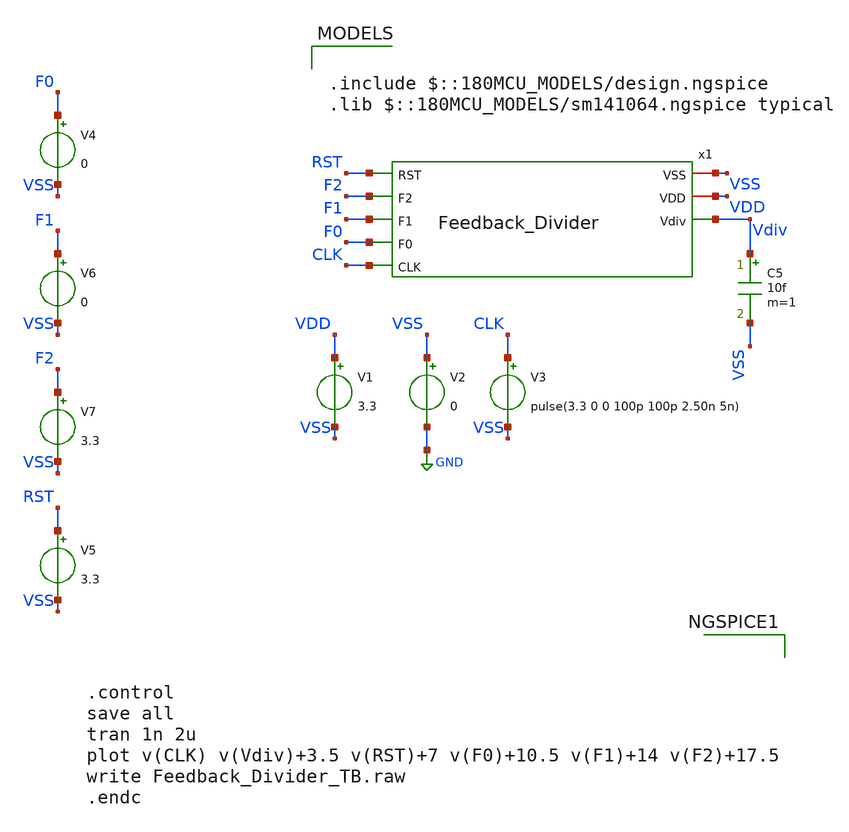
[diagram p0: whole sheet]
** sch_path: Clock_Generator_PAKISTAN_02/Schematics/delete.sch
**.subckt delete
V1 VDD VSS 3.3
V2 VSS GND 0
V3 CLK VSS pulse(3.3 0 0 100p 100p 2.50n 5n)
C5 Vdiv VSS 10f m=1
V5 RST VSS 3.3
x1 VSS VDD RST Vdiv F2 F1 F0 CLK Feedback_Divider
V4 F0 VSS 0
V6 F1 VSS 0
V7 F2 VSS 3.3
**** begin user architecture code

.include $::180MCU_MODELS/design.ngspice
.lib $::180MCU_MODELS/sm141064.ngspice typical




.control
save all
tran 1n 2u
plot v(CLK) v(Vdiv)+3.5 v(RST)+7 v(F0)+10.5 v(F1)+14 v(F2)+17.5
write Feedback_Divider_TB.raw
.endc


**** end user architecture code
**.ends
.GLOBAL GND
.end
